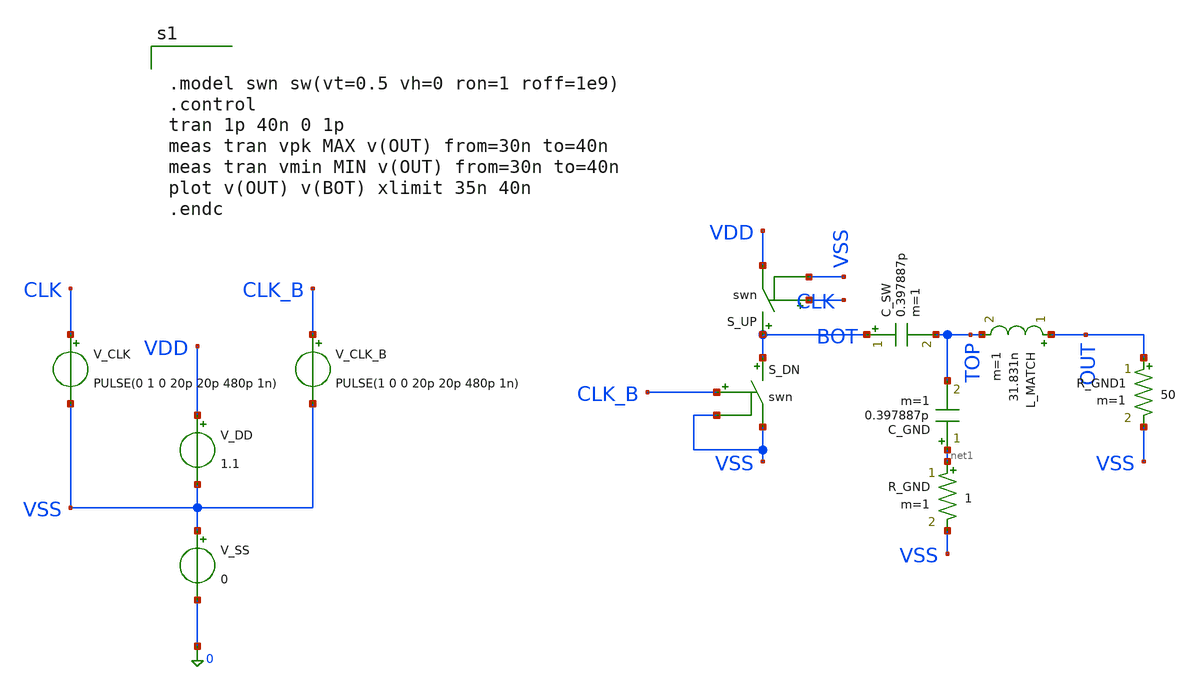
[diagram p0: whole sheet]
** sch_path: tx_am_scpa/scpa_x.sch
**.subckt scpa_x
V_DD VDD VSS 1.1
V_CLK CLK VSS PULSE(0 1 0 20p 20p 480p 1n)
V_CLK_B CLK_B VSS PULSE(1 0 0 20p 20p 480p 1n)
S_UP BOT VDD CLK VSS swn
S_DN BOT VSS CLK_B VSS swn
C_SW BOT TOP 0.397887p m=1
C_GND net1 TOP 0.397887p m=1
R_GND net1 VSS 1 m=1
L_MATCH OUT TOP 31.831n m=1
R_GND1 OUT VSS 50 m=1
V_SS VSS 0 0
**** begin user architecture code


.model swn sw(vt=0.5 vh=0 ron=1 roff=1e9)
.control
tran 1p 40n 0 1p
meas tran vpk MAX v(OUT) from=30n to=40n
meas tran vmin MIN v(OUT) from=30n to=40n
plot v(OUT) v(BOT) xlimit 35n 40n
.endc


**** end user architecture code
**.ends
**** begin user architecture code
.MODEL SW1 SW   VT=0.9 VH=0.01  RON=0.01 ROFF=10G
**** end user architecture code
.end
